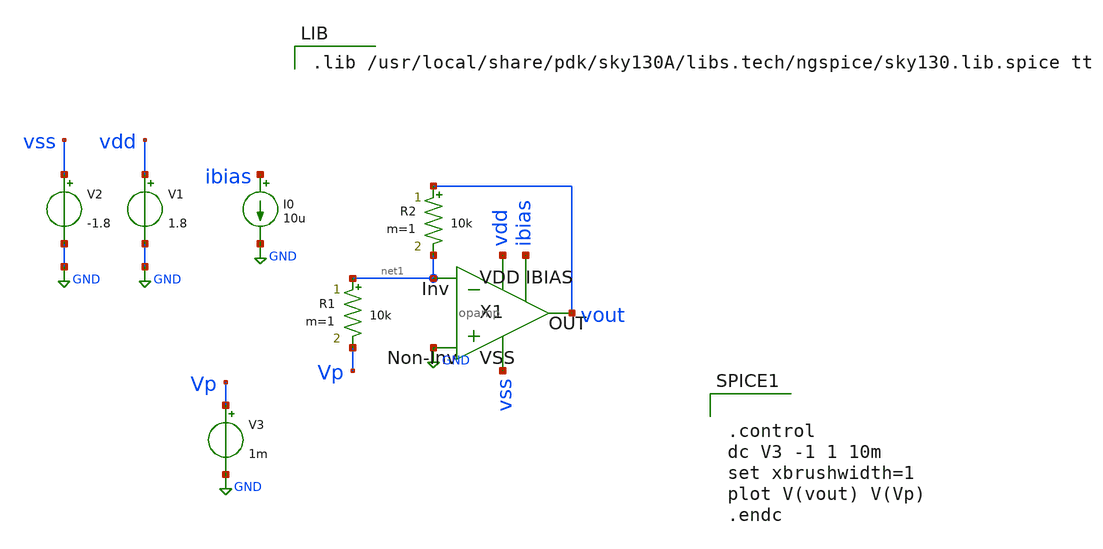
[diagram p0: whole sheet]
** sch_path: Fractional Order PID/OPAMP/opamp_tb.sch
**.subckt opamp_tb
V1 vdd GND 1.8
V3 Vp GND 1m
X1 net1 GND vss vdd vout ibias opamp
I0 ibias GND 10u
R1 net1 Vp 10k m=1
R2 vout net1 10k m=1
V2 vss GND -1.8
**** begin user architecture code

.lib /usr/local/share/pdk/sky130A/libs.tech/ngspice/sky130.lib.spice tt



.control
dc V3 -1 1 10m
set xbrushwidth=1
plot V(vout) V(Vp)
.endc


**** end user architecture code
**.ends

* expanding   symbol:  /home/parallels/OPAMP/opamp.sym # of pins=6
** sym_path: /home/parallels/OPAMP/opamp.sym
** sch_path: /home/parallels/OPAMP/opamp.sch
.subckt opamp VN VP GND VDD VOUT IBIAS
*.iopin VDD
*.iopin IBIAS
*.ipin VN
*.ipin VP
*.iopin GND
*.opin VOUT
XM1 IBIAS IBIAS VDD VDD sky130_fd_pr__pfet_01v8 L=0.3 W=3 nf=1 ad='int((nf+1)/2) * W/nf * 0.29' as='int((nf+2)/2) * W/nf * 0.29'
+ pd='2*int((nf+1)/2) * (W/nf + 0.29)' ps='2*int((nf+2)/2) * (W/nf + 0.29)' nrd='0.29 / W' nrs='0.29 / W'
+ sa=0 sb=0 sd=0 mult=1 m=1
XM2 net1 IBIAS VDD VDD sky130_fd_pr__pfet_01v8 L=0.3 W=30 nf=5 ad='int((nf+1)/2) * W/nf * 0.29' as='int((nf+2)/2) * W/nf * 0.29'
+ pd='2*int((nf+1)/2) * (W/nf + 0.29)' ps='2*int((nf+2)/2) * (W/nf + 0.29)' nrd='0.29 / W' nrs='0.29 / W'
+ sa=0 sb=0 sd=0 mult=1 m=1
XM3 net2 VN net1 VDD sky130_fd_pr__pfet_01v8 L=0.3 W=36 nf=6 ad='int((nf+1)/2) * W/nf * 0.29' as='int((nf+2)/2) * W/nf * 0.29'
+ pd='2*int((nf+1)/2) * (W/nf + 0.29)' ps='2*int((nf+2)/2) * (W/nf + 0.29)' nrd='0.29 / W' nrs='0.29 / W'
+ sa=0 sb=0 sd=0 mult=1 m=1
XM4 o1 VP net1 VDD sky130_fd_pr__pfet_01v8 L=0.3 W=36 nf=6 ad='int((nf+1)/2) * W/nf * 0.29' as='int((nf+2)/2) * W/nf * 0.29'
+ pd='2*int((nf+1)/2) * (W/nf + 0.29)' ps='2*int((nf+2)/2) * (W/nf + 0.29)' nrd='0.29 / W' nrs='0.29 / W'
+ sa=0 sb=0 sd=0 mult=1 m=1
XM5 net2 net2 GND GND sky130_fd_pr__nfet_01v8 L=0.3 W=6 nf=2 ad='int((nf+1)/2) * W/nf * 0.29' as='int((nf+2)/2) * W/nf * 0.29'
+ pd='2*int((nf+1)/2) * (W/nf + 0.29)' ps='2*int((nf+2)/2) * (W/nf + 0.29)' nrd='0.29 / W' nrs='0.29 / W'
+ sa=0 sb=0 sd=0 mult=1 m=1
XM6 o1 net2 GND GND sky130_fd_pr__nfet_01v8 L=0.3 W=6 nf=2 ad='int((nf+1)/2) * W/nf * 0.29' as='int((nf+2)/2) * W/nf * 0.29'
+ pd='2*int((nf+1)/2) * (W/nf + 0.29)' ps='2*int((nf+2)/2) * (W/nf + 0.29)' nrd='0.29 / W' nrs='0.29 / W'
+ sa=0 sb=0 sd=0 mult=1 m=1
XM7 VOUT IBIAS VDD VDD sky130_fd_pr__pfet_01v8 L=0.3 W=45 nf=9 ad='int((nf+1)/2) * W/nf * 0.29' as='int((nf+2)/2) * W/nf * 0.29'
+ pd='2*int((nf+1)/2) * (W/nf + 0.29)' ps='2*int((nf+2)/2) * (W/nf + 0.29)' nrd='0.29 / W' nrs='0.29 / W'
+ sa=0 sb=0 sd=0 mult=1 m=1
XM8 VOUT o1 GND GND sky130_fd_pr__nfet_01v8 L=0.3 W=18 nf=3 ad='int((nf+1)/2) * W/nf * 0.29' as='int((nf+2)/2) * W/nf * 0.29'
+ pd='2*int((nf+1)/2) * (W/nf + 0.29)' ps='2*int((nf+2)/2) * (W/nf + 0.29)' nrd='0.29 / W' nrs='0.29 / W'
+ sa=0 sb=0 sd=0 mult=1 m=1
XC2 o1 VOUT sky130_fd_pr__cap_mim_m3_1 W=11 L=22 MF=1 m=1
.ends

.GLOBAL GND
.end
